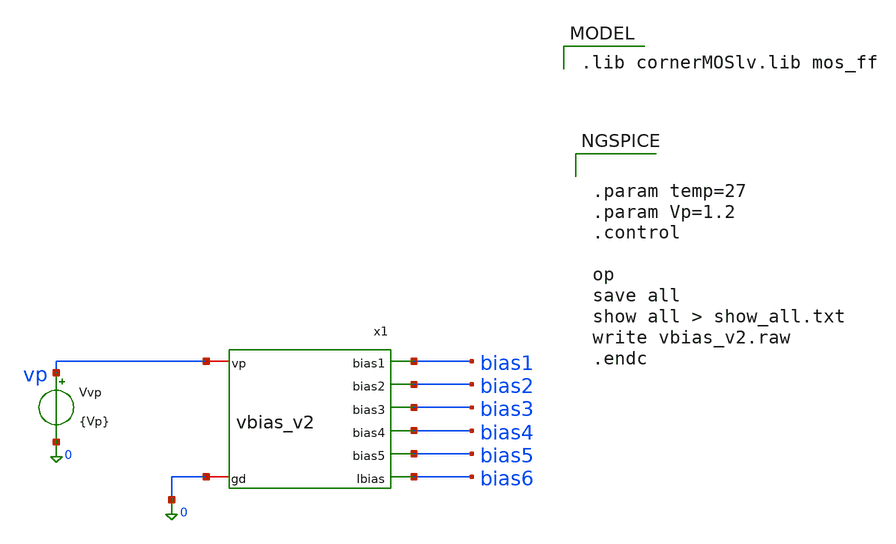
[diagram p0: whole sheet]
** sch_path: PLL0663-main/schematic/xschem/charge_pump/vbias/vbias_v2_tb.sch
**.subckt vbias_v2_tb
Vvp vp 0 {Vp}
x1 vp bias2 bias3 bias1 bias4 bias5 bias6 0 vbias_v2
**** begin user architecture code
 .lib cornerMOSlv.lib mos_ff



.param temp=27
.param Vp=1.2
.control

op
save all
show all > show_all.txt
write vbias_v2.raw
.endc


**** end user architecture code
**.ends
.end
